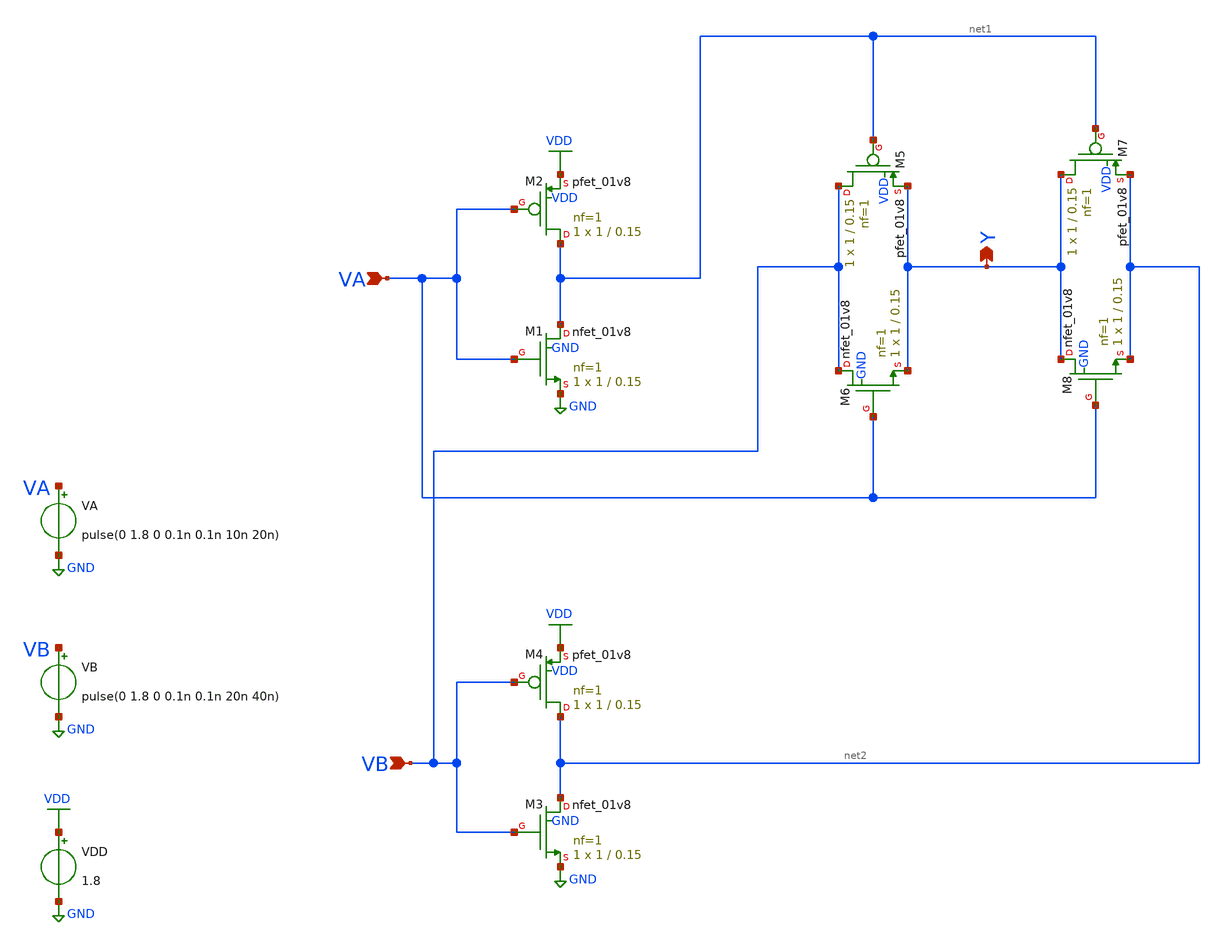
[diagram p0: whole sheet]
** sch_path: units/top/ana/cells/xor/xor_TG.sch
**.subckt xor_TG VA VB Y
*.ipin VA
*.ipin VB
*.opin Y
XM1 net1 VA GND GND sky130_fd_pr__nfet_01v8 L=0.15 W=1 nf=1 ad='int((1 + 1)/2) * 1 / 1 * 0.29' as='int((1 + 2)/2) * 1 / 1 * 0.29'
+ pd='2*int((1 + 1)/2) * (1 / 1 + 0.29)' ps='2*int((1 + 2)/2) * (1 / 1 + 0.29)' nrd='0.29 / 1 ' nrs='0.29 / 1 '
+ sa=0 sb=0 sd=0 mult=1 m=1
XM2 net1 VA VDD VDD sky130_fd_pr__pfet_01v8 L=0.15 W=1 nf=1 ad='int((1 + 1)/2) * 1 / 1 * 0.29' as='int((1 + 2)/2) * 1 / 1 * 0.29'
+ pd='2*int((1 + 1)/2) * (1 / 1 + 0.29)' ps='2*int((1 + 2)/2) * (1 / 1 + 0.29)' nrd='0.29 / 1 ' nrs='0.29 / 1 '
+ sa=0 sb=0 sd=0 mult=1 m=1
XM3 net2 VB GND GND sky130_fd_pr__nfet_01v8 L=0.15 W=1 nf=1 ad='int((1 + 1)/2) * 1 / 1 * 0.29' as='int((1 + 2)/2) * 1 / 1 * 0.29'
+ pd='2*int((1 + 1)/2) * (1 / 1 + 0.29)' ps='2*int((1 + 2)/2) * (1 / 1 + 0.29)' nrd='0.29 / 1 ' nrs='0.29 / 1 '
+ sa=0 sb=0 sd=0 mult=1 m=1
XM4 net2 VB VDD VDD sky130_fd_pr__pfet_01v8 L=0.15 W=1 nf=1 ad='int((1 + 1)/2) * 1 / 1 * 0.29' as='int((1 + 2)/2) * 1 / 1 * 0.29'
+ pd='2*int((1 + 1)/2) * (1 / 1 + 0.29)' ps='2*int((1 + 2)/2) * (1 / 1 + 0.29)' nrd='0.29 / 1 ' nrs='0.29 / 1 '
+ sa=0 sb=0 sd=0 mult=1 m=1
XM5 VB net1 Y VDD sky130_fd_pr__pfet_01v8 L=0.15 W=1 nf=1 ad='int((1 + 1)/2) * 1 / 1 * 0.29' as='int((1 + 2)/2) * 1 / 1 * 0.29'
+ pd='2*int((1 + 1)/2) * (1 / 1 + 0.29)' ps='2*int((1 + 2)/2) * (1 / 1 + 0.29)' nrd='0.29 / 1 ' nrs='0.29 / 1 '
+ sa=0 sb=0 sd=0 mult=1 m=1
XM6 VB VA Y GND sky130_fd_pr__nfet_01v8 L=0.15 W=1 nf=1 ad='int((1 + 1)/2) * 1 / 1 * 0.29' as='int((1 + 2)/2) * 1 / 1 * 0.29'
+ pd='2*int((1 + 1)/2) * (1 / 1 + 0.29)' ps='2*int((1 + 2)/2) * (1 / 1 + 0.29)' nrd='0.29 / 1 ' nrs='0.29 / 1 '
+ sa=0 sb=0 sd=0 mult=1 m=1
XM7 Y net1 net2 VDD sky130_fd_pr__pfet_01v8 L=0.15 W=1 nf=1 ad='int((1 + 1)/2) * 1 / 1 * 0.29' as='int((1 + 2)/2) * 1 / 1 * 0.29'
+ pd='2*int((1 + 1)/2) * (1 / 1 + 0.29)' ps='2*int((1 + 2)/2) * (1 / 1 + 0.29)' nrd='0.29 / 1 ' nrs='0.29 / 1 '
+ sa=0 sb=0 sd=0 mult=1 m=1
XM8 Y VA net2 GND sky130_fd_pr__nfet_01v8 L=0.15 W=1 nf=1 ad='int((1 + 1)/2) * 1 / 1 * 0.29' as='int((1 + 2)/2) * 1 / 1 * 0.29'
+ pd='2*int((1 + 1)/2) * (1 / 1 + 0.29)' ps='2*int((1 + 2)/2) * (1 / 1 + 0.29)' nrd='0.29 / 1 ' nrs='0.29 / 1 '
+ sa=0 sb=0 sd=0 mult=1 m=1
VB VB GND pulse(0 1.8 0 0.1n 0.1n 20n 40n)
VA VA GND pulse(0 1.8 0 0.1n 0.1n 10n 20n)
VDD VDD GND 1.8
.save i(vdd)
**** begin user architecture code

.lib /usr/local/share/pdk/sky130B/libs.tech/ngspice/sky130.lib.spice tt
.option wnflag=1

**** end user architecture code
**.ends
.GLOBAL VDD
.GLOBAL GND
**** begin user architecture code


.save v(VA) v(VB) v(Y)
.tran 0.1n 200n


**** end user architecture code
.end
